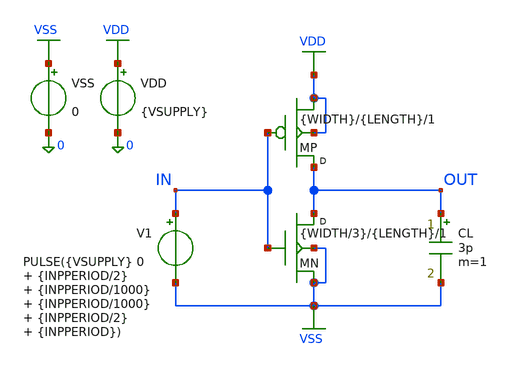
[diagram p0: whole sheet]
** sch_path: docs/assets/circuits/cmos_inverter.sch
**.subckt cmos_inverter
MN OUT IN VSS VSS NMOS w={WIDTH/3} l={LENGTH} m=1
MP OUT IN VDD VDD PMOS w={WIDTH} l={LENGTH} m=1
VDD VDD 0 {VSUPPLY}
VSS VSS 0 0
V1 IN VSS PULSE({VSUPPLY} 0 {INPPERIOD/2} {INPPERIOD/1000} {INPPERIOD/1000} {INPPERIOD/2} {INPPERIOD})
CL OUT VSS 3p m=1
**.ends
.GLOBAL VDD
.GLOBAL VSS
.end
